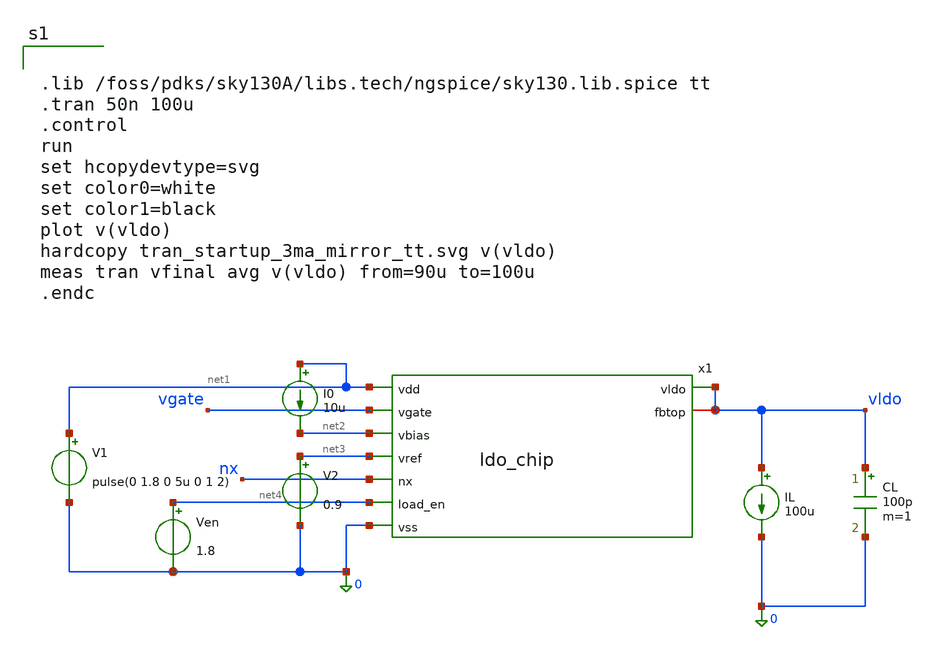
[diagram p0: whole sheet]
** sch_path: src/schematics/ldo_tran.sch
**.subckt ldo_tran
I0 net1 net2 10u
V1 net1 0 pulse(0 1.8 0 5u 0 1 2)
V2 net3 0 0.9
Ven net4 0 1.8
CL vldo 0 100p m=1
IL vldo 0 100u
x1 net1 vgate net2 net3 vldo vldo nx net4 0 ldo_chip
**** begin user architecture code


.lib /foss/pdks/sky130A/libs.tech/ngspice/sky130.lib.spice tt
.tran 50n 100u
.control
run
set hcopydevtype=svg
set color0=white
set color1=black
plot v(vldo)
hardcopy tran_startup_3ma_mirror_tt.svg v(vldo)
meas tran vfinal avg v(vldo) from=90u to=100u
.endc


**** end user architecture code
**.ends
.end
